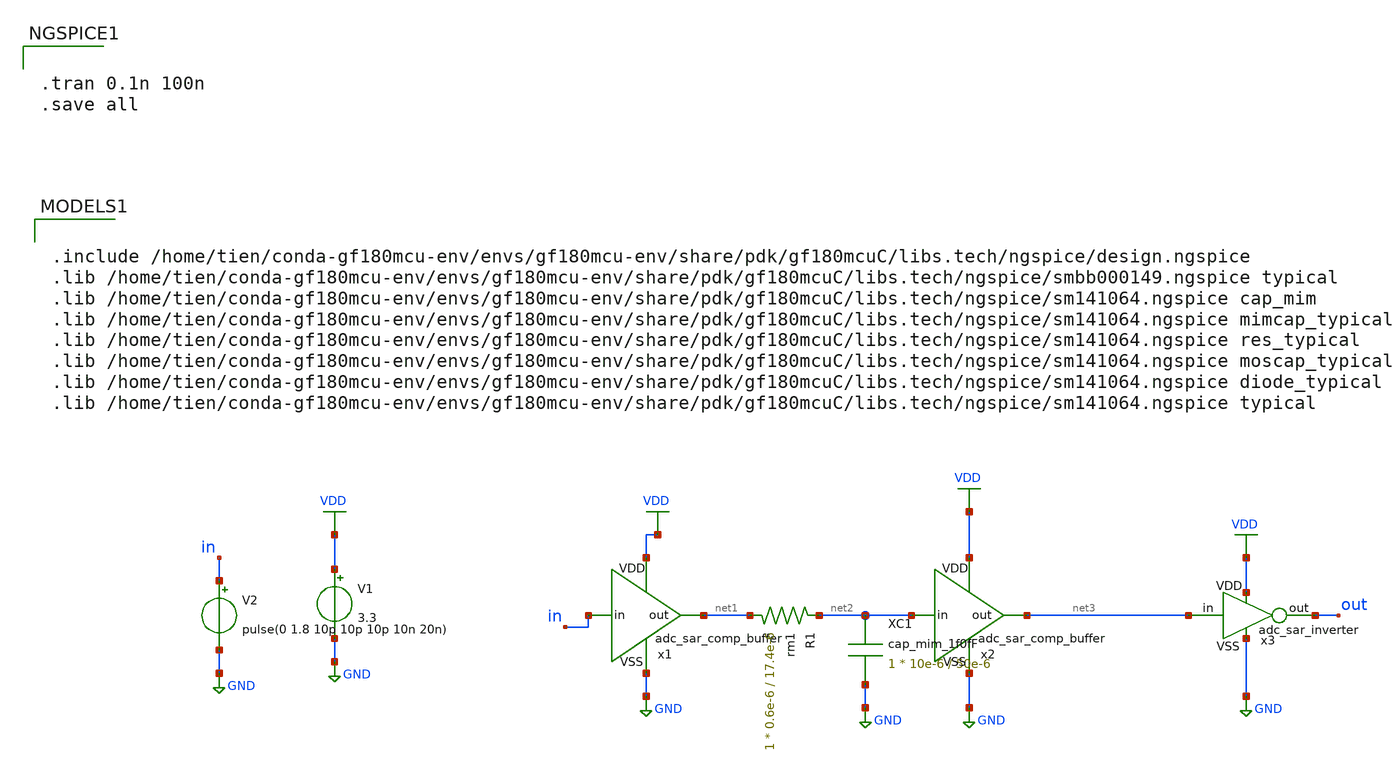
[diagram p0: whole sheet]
** sch_path: tesst3.sch
**.subckt tesst3
V1 VDD GND 3.3
V2 in GND pulse(0 1.8 10p 10p 10p 10n 20n)
x1 VDD GND in net1 adc_sar_comp_buffer
XC1 net2 GND cap_mim_1f0fF c_width=10e-6 c_length=50e-6 m=1
XR1 net1 net2 rm1 r_width=0.6e-6 r_length=17.4e-6 m=1
x2 VDD GND net2 net3 adc_sar_comp_buffer
x3 VDD GND net3 out adc_sar_inverter
**** begin user architecture code


.tran 0.1n 100n
.save all



.include /home/tien/conda-gf180mcu-env/envs/gf180mcu-env/share/pdk/gf180mcuC/libs.tech/ngspice/design.ngspice
.lib /home/tien/conda-gf180mcu-env/envs/gf180mcu-env/share/pdk/gf180mcuC/libs.tech/ngspice/smbb000149.ngspice typical
.lib /home/tien/conda-gf180mcu-env/envs/gf180mcu-env/share/pdk/gf180mcuC/libs.tech/ngspice/sm141064.ngspice cap_mim
.lib /home/tien/conda-gf180mcu-env/envs/gf180mcu-env/share/pdk/gf180mcuC/libs.tech/ngspice/sm141064.ngspice mimcap_typical
.lib /home/tien/conda-gf180mcu-env/envs/gf180mcu-env/share/pdk/gf180mcuC/libs.tech/ngspice/sm141064.ngspice res_typical
.lib /home/tien/conda-gf180mcu-env/envs/gf180mcu-env/share/pdk/gf180mcuC/libs.tech/ngspice/sm141064.ngspice moscap_typical
.lib /home/tien/conda-gf180mcu-env/envs/gf180mcu-env/share/pdk/gf180mcuC/libs.tech/ngspice/sm141064.ngspice diode_typical
.lib /home/tien/conda-gf180mcu-env/envs/gf180mcu-env/share/pdk/gf180mcuC/libs.tech/ngspice/sm141064.ngspice typical

**** end user architecture code
**.ends

* expanding   symbol:  adc_sar_comp_buffer.sym # of pins=4
** sym_path: adc_sar_comp_buffer.sym
** sch_path: adc_sar_comp_buffer.sch
.subckt adc_sar_comp_buffer VDD VSS in out
*.iopin VDD
*.iopin VSS
*.ipin in
*.opin out
XM1 buf_mid in VSS VSS nfet_03v3 L=0.28u W=0.5u nf=1 ad='int((nf+1)/2) * W/nf * 0.18u' as='int((nf+2)/2) * W/nf * 0.18u'
+ pd='2*int((nf+1)/2) * (W/nf + 0.18u)' ps='2*int((nf+2)/2) * (W/nf + 0.18u)' nrd='0.18u / W' nrs='0.18u / W'
+ sa=0 sb=0 sd=0 m=1
XM2 out buf_mid VSS VSS nfet_03v3 L=0.28u W=1u nf=1 ad='int((nf+1)/2) * W/nf * 0.18u' as='int((nf+2)/2) * W/nf * 0.18u'
+ pd='2*int((nf+1)/2) * (W/nf + 0.18u)' ps='2*int((nf+2)/2) * (W/nf + 0.18u)' nrd='0.18u / W' nrs='0.18u / W'
+ sa=0 sb=0 sd=0 m=1
XM3 buf_mid in VDD VDD pfet_03v3 L=0.28u W=1u nf=1 ad='int((nf+1)/2) * W/nf * 0.18u' as='int((nf+2)/2) * W/nf * 0.18u'
+ pd='2*int((nf+1)/2) * (W/nf + 0.18u)' ps='2*int((nf+2)/2) * (W/nf + 0.18u)' nrd='0.18u / W' nrs='0.18u / W'
+ sa=0 sb=0 sd=0 m=1
XM4 out buf_mid VDD VDD pfet_03v3 L=0.28u W=2u nf=1 ad='int((nf+1)/2) * W/nf * 0.18u' as='int((nf+2)/2) * W/nf * 0.18u'
+ pd='2*int((nf+1)/2) * (W/nf + 0.18u)' ps='2*int((nf+2)/2) * (W/nf + 0.18u)' nrd='0.18u / W' nrs='0.18u / W'
+ sa=0 sb=0 sd=0 m=1
.ends


* expanding   symbol:  adc_sar_inverter.sym # of pins=4
** sym_path: adc_sar_inverter.sym
** sch_path: adc_sar_inverter.sch
.subckt adc_sar_inverter VDD VSS in out
*.iopin VDD
*.iopin VSS
*.ipin in
*.opin out
XM1 out in VSS VSS nfet_03v3 L=0.28u W=0.42u nf=1 ad='int((nf+1)/2) * W/nf * 0.18u' as='int((nf+2)/2) * W/nf * 0.18u'
+ pd='2*int((nf+1)/2) * (W/nf + 0.18u)' ps='2*int((nf+2)/2) * (W/nf + 0.18u)' nrd='0.18u / W' nrs='0.18u / W'
+ sa=0 sb=0 sd=0 m=1
XM2 out in VDD VDD pfet_03v3 L=0.28u W=0.84u nf=1 ad='int((nf+1)/2) * W/nf * 0.18u' as='int((nf+2)/2) * W/nf * 0.18u'
+ pd='2*int((nf+1)/2) * (W/nf + 0.18u)' ps='2*int((nf+2)/2) * (W/nf + 0.18u)' nrd='0.18u / W' nrs='0.18u / W'
+ sa=0 sb=0 sd=0 m=1
.ends

.GLOBAL VDD
.GLOBAL GND
.end
